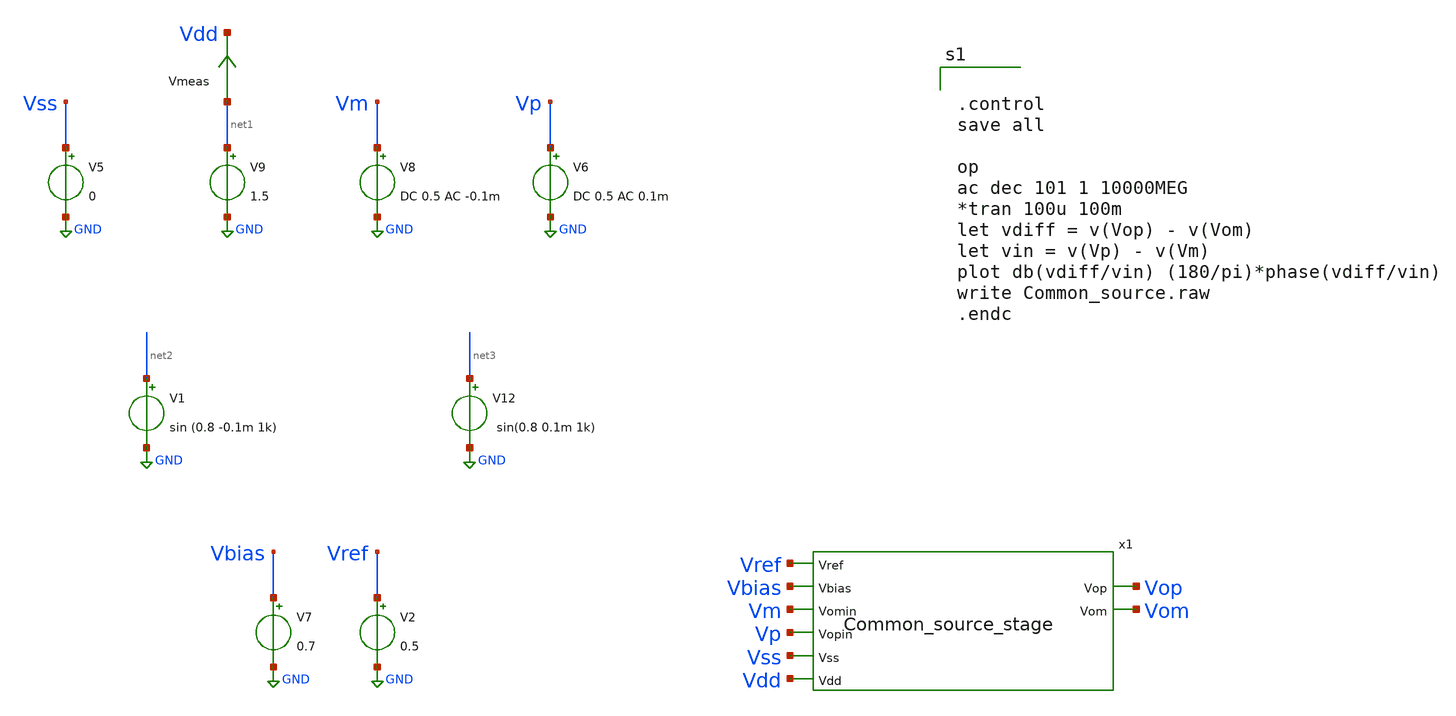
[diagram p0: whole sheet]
** sch_path: src/Opamp_Design/testbenches/Common_Source_Stage_tb.sch
**.subckt Common_Source_Stage_tb
V8 Vm GND DC 0.5 AC -0.1m
V6 Vp GND DC 0.5 AC 0.1m
V9 net1 GND 1.5
Vmeas net1 Vdd 0
.save i(vmeas)
V1 net2 GND sin (0.8 -0.1m 1k)
V12 net3 GND sin(0.8 0.1m 1k)
V5 Vss GND 0
V7 Vbias GND 0.7
x1 Vref Vbias Vm Vp Vss Vdd Vop Vom Common_source_stage
V2 Vref GND 0.5
**** begin user architecture code

** opencircuitdesign pdks install
.lib $::SKYWATER_MODELS/sky130.lib.spice tt




.control
save all

op
ac dec 101 1 10000MEG
*tran 100u 100m
let vdiff = v(Vop) - v(Vom)
let vin = v(Vp) - v(Vm)
plot db(vdiff/vin) (180/pi)*phase(vdiff/vin)
write Common_source.raw
.endc


**** end user architecture code
**.ends

* expanding   symbol:  /foss/designs/FYP/Sky130_Multiplier/Opamp_Design/src/Common_source_stage.sym
*+ # of pins=8
** sym_path: src/Opamp_Design/src/Common_source_stage.sym
** sch_path: src/Opamp_Design/src/Common_source_stage.sch
.subckt Common_source_stage Vref Vbias Vomin Vopin Vss Vdd Vop Vom
*.ipin Vdd
*.opin Vop
*.ipin Vss
*.opin Vom
*.ipin Vopin
*.ipin Vomin
*.ipin Vbias
*.ipin Vref
XM9 Vop Vopin Vdd Vdd sky130_fd_pr__pfet_01v8_lvt L=1 W=2 nf=1 ad='int((nf+1)/2) * W/nf * 0.29' as='int((nf+2)/2) * W/nf * 0.29'
+ pd='2*int((nf+1)/2) * (W/nf + 0.29)' ps='2*int((nf+2)/2) * (W/nf + 0.29)' nrd='0.29 / W' nrs='0.29 / W'
+ sa=0 sb=0 sd=0 mult=9 m=9
XM4 Vom Vomin Vdd Vdd sky130_fd_pr__pfet_01v8_lvt L=1 W=2 nf=1 ad='int((nf+1)/2) * W/nf * 0.29' as='int((nf+2)/2) * W/nf * 0.29'
+ pd='2*int((nf+1)/2) * (W/nf + 0.29)' ps='2*int((nf+2)/2) * (W/nf + 0.29)' nrd='0.29 / W' nrs='0.29 / W'
+ sa=0 sb=0 sd=0 mult=9 m=9
XM2 Vop Vout Vss Vss sky130_fd_pr__nfet_01v8_lvt L=1 W=1 nf=1 ad='int((nf+1)/2) * W/nf * 0.29' as='int((nf+2)/2) * W/nf * 0.29'
+ pd='2*int((nf+1)/2) * (W/nf + 0.29)' ps='2*int((nf+2)/2) * (W/nf + 0.29)' nrd='0.29 / W' nrs='0.29 / W'
+ sa=0 sb=0 sd=0 mult=9 m=9
XM1 Vom Vout Vss Vss sky130_fd_pr__nfet_01v8_lvt L=1 W=1 nf=1 ad='int((nf+1)/2) * W/nf * 0.29' as='int((nf+2)/2) * W/nf * 0.29'
+ pd='2*int((nf+1)/2) * (W/nf + 0.29)' ps='2*int((nf+2)/2) * (W/nf + 0.29)' nrd='0.29 / W' nrs='0.29 / W'
+ sa=0 sb=0 sd=0 mult=9 m=9
XM3 net1 Vbiasp Vdd Vdd sky130_fd_pr__pfet_01v8_lvt L=5 W=1 nf=1 ad='int((nf+1)/2) * W/nf * 0.29' as='int((nf+2)/2) * W/nf * 0.29'
+ pd='2*int((nf+1)/2) * (W/nf + 0.29)' ps='2*int((nf+2)/2) * (W/nf + 0.29)' nrd='0.29 / W' nrs='0.29 / W'
+ sa=0 sb=0 sd=0 mult=2 m=2
XM7 Vtest Vcm net1 Vdd sky130_fd_pr__pfet_01v8_lvt L=10 W=1 nf=1 ad='int((nf+1)/2) * W/nf * 0.29' as='int((nf+2)/2) * W/nf * 0.29'
+ pd='2*int((nf+1)/2) * (W/nf + 0.29)' ps='2*int((nf+2)/2) * (W/nf + 0.29)' nrd='0.29 / W' nrs='0.29 / W'
+ sa=0 sb=0 sd=0 mult=2 m=2
XM8 Vout Vref net1 Vdd sky130_fd_pr__pfet_01v8_lvt L=10 W=1 nf=1 ad='int((nf+1)/2) * W/nf * 0.29' as='int((nf+2)/2) * W/nf * 0.29'
+ pd='2*int((nf+1)/2) * (W/nf + 0.29)' ps='2*int((nf+2)/2) * (W/nf + 0.29)' nrd='0.29 / W' nrs='0.29 / W'
+ sa=0 sb=0 sd=0 mult=2 m=2
XM5 Vtest Vtest Vss Vss sky130_fd_pr__nfet_01v8_lvt L=20 W=0.5 nf=1 ad='int((nf+1)/2) * W/nf * 0.29'
+ as='int((nf+2)/2) * W/nf * 0.29' pd='2*int((nf+1)/2) * (W/nf + 0.29)' ps='2*int((nf+2)/2) * (W/nf + 0.29)'
+ nrd='0.29 / W' nrs='0.29 / W' sa=0 sb=0 sd=0 mult=2 m=2
XM6 Vout Vtest Vss Vss sky130_fd_pr__nfet_01v8_lvt L=20 W=0.5 nf=1 ad='int((nf+1)/2) * W/nf * 0.29' as='int((nf+2)/2) * W/nf * 0.29'
+ pd='2*int((nf+1)/2) * (W/nf + 0.29)' ps='2*int((nf+2)/2) * (W/nf + 0.29)' nrd='0.29 / W' nrs='0.29 / W'
+ sa=0 sb=0 sd=0 mult=2 m=2
x1 Vop Vcm res_pack
x2 Vcm Vom res_pack
XM10 Vbias Vbias Vss Vss sky130_fd_pr__nfet_01v8_lvt L=1 W=0.6 nf=1 ad='int((nf+1)/2) * W/nf * 0.29'
+ as='int((nf+2)/2) * W/nf * 0.29' pd='2*int((nf+1)/2) * (W/nf + 0.29)' ps='2*int((nf+2)/2) * (W/nf + 0.29)'
+ nrd='0.29 / W' nrs='0.29 / W' sa=0 sb=0 sd=0 mult=2 m=2
XM11 Vbiasp Vbias Vss Vss sky130_fd_pr__nfet_01v8_lvt L=1 W=0.6 nf=1 ad='int((nf+1)/2) * W/nf * 0.29'
+ as='int((nf+2)/2) * W/nf * 0.29' pd='2*int((nf+1)/2) * (W/nf + 0.29)' ps='2*int((nf+2)/2) * (W/nf + 0.29)'
+ nrd='0.29 / W' nrs='0.29 / W' sa=0 sb=0 sd=0 mult=2 m=2
XM12 Vbiasp Vbiasp Vdd Vdd sky130_fd_pr__pfet_01v8_lvt L=1 W=6 nf=1 ad='int((nf+1)/2) * W/nf * 0.29'
+ as='int((nf+2)/2) * W/nf * 0.29' pd='2*int((nf+1)/2) * (W/nf + 0.29)' ps='2*int((nf+2)/2) * (W/nf + 0.29)'
+ nrd='0.29 / W' nrs='0.29 / W' sa=0 sb=0 sd=0 mult=2 m=2
.ends


* expanding   symbol:  /foss/designs/FYP/Sky130_Design/Opamp_Design/src/res_pack.sym # of pins=2
** sym_path: src/Opamp_Design/src/res_pack.sym
** sch_path: src/Opamp_Design/src/res_pack.sch
.subckt res_pack Vin Vout
*.ipin Vin
*.opin Vout
XR1 net4 Vin sky130_fd_pr__res_generic_po W=0.5 L=40 m=1
XR2 net5 net4 sky130_fd_pr__res_generic_po W=0.5 L=40 m=1
XR3 net6 net5 sky130_fd_pr__res_generic_po W=0.5 L=40 m=1
XR4 net7 net6 sky130_fd_pr__res_generic_po W=0.5 L=40 m=1
XR5 net1 net7 sky130_fd_pr__res_generic_po W=0.5 L=40 m=1
XR6 net8 net2 sky130_fd_pr__res_generic_po W=0.5 L=40 m=1
XR7 net9 net8 sky130_fd_pr__res_generic_po W=0.5 L=40 m=1
XR8 net10 net9 sky130_fd_pr__res_generic_po W=0.5 L=40 m=1
XR9 net11 net10 sky130_fd_pr__res_generic_po W=0.5 L=40 m=1
XR10 net1 net11 sky130_fd_pr__res_generic_po W=0.5 L=40 m=1
XR11 net12 net2 sky130_fd_pr__res_generic_po W=0.5 L=40 m=1
XR12 net13 net12 sky130_fd_pr__res_generic_po W=0.5 L=40 m=1
XR13 net14 net13 sky130_fd_pr__res_generic_po W=0.5 L=40 m=1
XR14 net15 net14 sky130_fd_pr__res_generic_po W=0.5 L=40 m=1
XR16 net16 Vout sky130_fd_pr__res_generic_po W=0.5 L=40 m=1
XR17 net17 net16 sky130_fd_pr__res_generic_po W=0.5 L=40 m=1
XR18 net18 net17 sky130_fd_pr__res_generic_po W=0.5 L=40 m=1
XR19 net19 net18 sky130_fd_pr__res_generic_po W=0.5 L=40 m=1
XR20 net3 net19 sky130_fd_pr__res_generic_po W=0.5 L=40 m=1
XR15 net3 net15 sky130_fd_pr__res_generic_po W=0.5 L=40 m=1
.ends

.GLOBAL GND
.end
